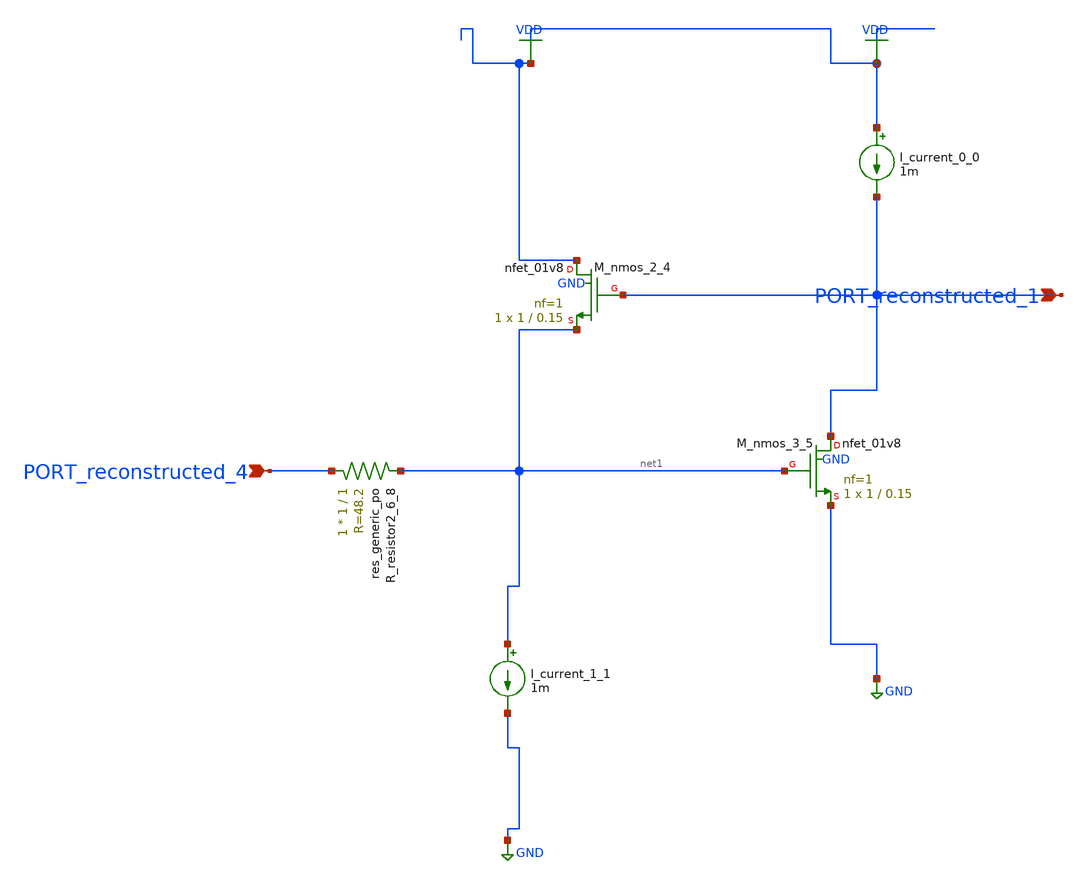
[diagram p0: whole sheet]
** sch_path: schematics/AMSNet/608.sch
**.subckt 608 PORT_reconstructed_1 PORT_reconstructed_4
*.ipin PORT_reconstructed_1
*.ipin PORT_reconstructed_4
I_current_0_0 VDD PORT_reconstructed_1 1m
I_current_1_1 net1 GND 1m
XM_nmos_2_4 VDD PORT_reconstructed_1 net1 GND sky130_fd_pr__nfet_01v8 L=0.15 W=1 nf=1 ad='int((1 + 1)/2) * 1 / 1 * 0.29'
+ as='int((1 + 2)/2) * 1 / 1 * 0.29' pd='2*int((1 + 1)/2) * (1 / 1 + 0.29)' ps='2*int((1 + 2)/2) * (1 / 1 + 0.29)'
+ nrd='0.29 / 1 ' nrs='0.29 / 1 ' sa=0 sb=0 sd=0 mult=1 m=1
XM_nmos_3_5 PORT_reconstructed_1 net1 GND GND sky130_fd_pr__nfet_01v8 L=0.15 W=1 nf=1 ad='int((1 + 1)/2) * 1 / 1 * 0.29'
+ as='int((1 + 2)/2) * 1 / 1 * 0.29' pd='2*int((1 + 1)/2) * (1 / 1 + 0.29)' ps='2*int((1 + 2)/2) * (1 / 1 + 0.29)'
+ nrd='0.29 / 1 ' nrs='0.29 / 1 ' sa=0 sb=0 sd=0 mult=1 m=1
XR_resistor2_6_8 PORT_reconstructed_4 net1 sky130_fd_pr__res_generic_po W=1 L=1 m=1
**.ends
.GLOBAL GND
.GLOBAL VDD
.end
